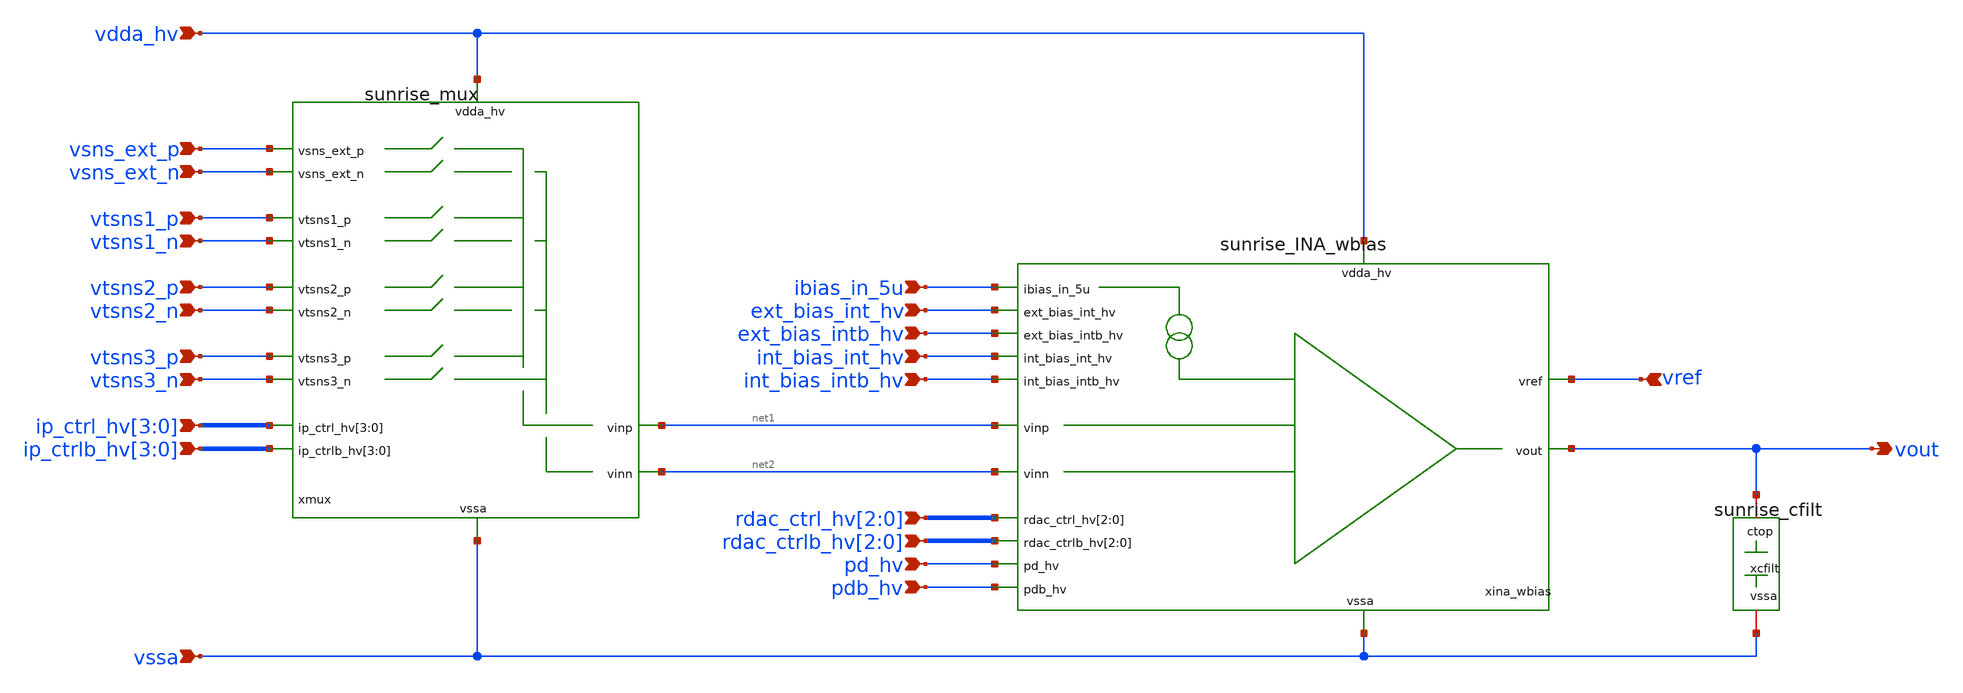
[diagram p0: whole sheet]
** sch_path: Schematics_Layout/sunrise_INA_top/sunrise_INA_top.sch
**.subckt sunrise_INA_top rdac_ctrl_hv[2],rdac_ctrl_hv[1],rdac_ctrl_hv[0]
*+ rdac_ctrlb_hv[2],rdac_ctrlb_hv[1],rdac_ctrlb_hv[0] pd_hv pdb_hv ext_bias_int_hv ext_bias_intb_hv int_bias_int_hv int_bias_intb_hv ibias_in_5u vdda_hv
*+ vssa vref vout ip_ctrl_hv[3],ip_ctrl_hv[2],ip_ctrl_hv[1],ip_ctrl_hv[0]
*+ ip_ctrlb_hv[3],ip_ctrlb_hv[2],ip_ctrlb_hv[1],ip_ctrlb_hv[0] vsns_ext_p vsns_ext_n vtsns1_p vtsns1_n vtsns2_p vtsns2_n vtsns3_p vtsns3_n
*.ipin rdac_ctrl_hv[2],rdac_ctrl_hv[1],rdac_ctrl_hv[0]
*.ipin rdac_ctrlb_hv[2],rdac_ctrlb_hv[1],rdac_ctrlb_hv[0]
*.ipin pd_hv
*.ipin pdb_hv
*.ipin ext_bias_int_hv
*.ipin ext_bias_intb_hv
*.ipin int_bias_int_hv
*.ipin int_bias_intb_hv
*.ipin ibias_in_5u
*.ipin vdda_hv
*.ipin vssa
*.ipin vref
*.opin vout
*.ipin ip_ctrl_hv[3],ip_ctrl_hv[2],ip_ctrl_hv[1],ip_ctrl_hv[0]
*.ipin ip_ctrlb_hv[3],ip_ctrlb_hv[2],ip_ctrlb_hv[1],ip_ctrlb_hv[0]
*.ipin vsns_ext_p
*.ipin vsns_ext_n
*.ipin vtsns1_p
*.ipin vtsns1_n
*.ipin vtsns2_p
*.ipin vtsns2_n
*.ipin vtsns3_p
*.ipin vtsns3_n
xcfilt vout vssa sunrise_cfilt
xmux vtsns1_p vdda_hv vssa ip_ctrl_hv[3] ip_ctrl_hv[2] ip_ctrl_hv[1] ip_ctrl_hv[0] ip_ctrlb_hv[3]
+ ip_ctrlb_hv[2] ip_ctrlb_hv[1] ip_ctrlb_hv[0] vtsns1_n vtsns2_p vtsns2_n vtsns3_p vtsns3_n vsns_ext_p net1 net2
+ vsns_ext_n sunrise_mux
xina_wbias vdda_hv ext_bias_int_hv ext_bias_intb_hv int_bias_int_hv int_bias_intb_hv ibias_in_5u
+ vref net1 vout net2 rdac_ctrl_hv[2] rdac_ctrl_hv[1] rdac_ctrl_hv[0] rdac_ctrlb_hv[2] rdac_ctrlb_hv[1]
+ rdac_ctrlb_hv[0] pd_hv pdb_hv vssa sunrise_INA_wbias
**.ends
.end
